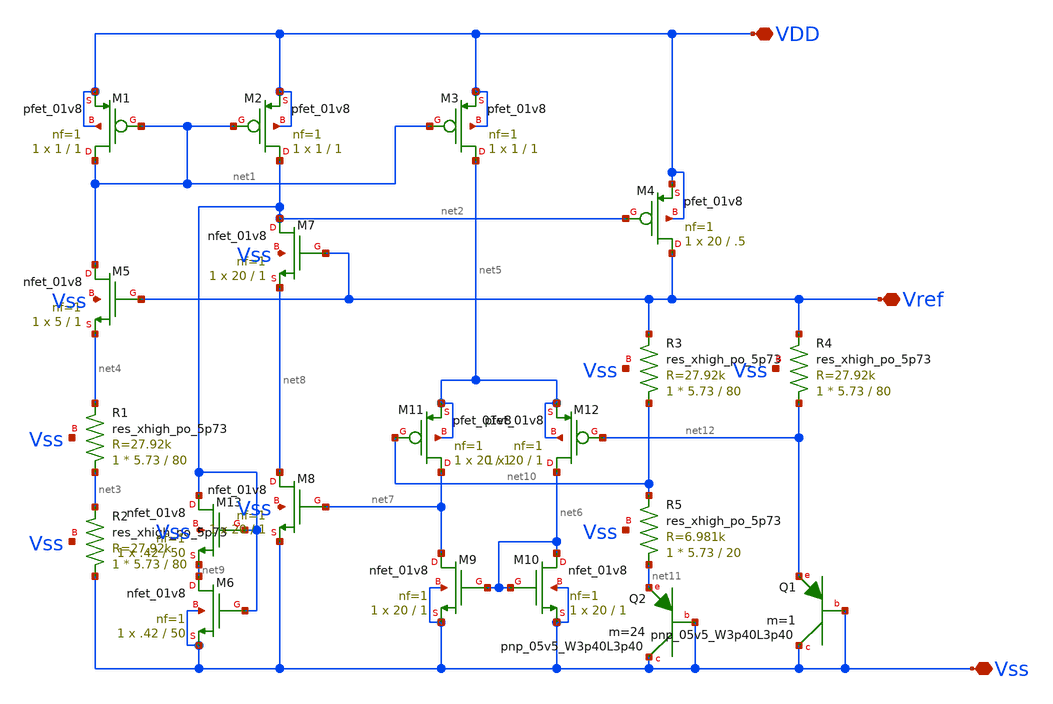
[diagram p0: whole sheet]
** sch_path: hw05/xschem/bandgap.sch
**.subckt bandgap VDD Vss Vref
*.iopin VDD
*.iopin Vss
*.iopin Vref
XM7 net2 Vref net8 Vss sky130_fd_pr__nfet_01v8 L=1 W=20 nf=1 ad='int((nf+1)/2) * W/nf * 0.29' as='int((nf+2)/2) * W/nf * 0.29'
+ pd='2*int((nf+1)/2) * (W/nf + 0.29)' ps='2*int((nf+2)/2) * (W/nf + 0.29)' nrd='0.29 / W' nrs='0.29 / W'
+ sa=0 sb=0 sd=0 mult=1 m=1
XM1 net1 net1 VDD VDD sky130_fd_pr__pfet_01v8 L=1 W=1 nf=1 ad='int((nf+1)/2) * W/nf * 0.29' as='int((nf+2)/2) * W/nf * 0.29'
+ pd='2*int((nf+1)/2) * (W/nf + 0.29)' ps='2*int((nf+2)/2) * (W/nf + 0.29)' nrd='0.29 / W' nrs='0.29 / W'
+ sa=0 sb=0 sd=0 mult=1 m=1
XM2 net2 net1 VDD VDD sky130_fd_pr__pfet_01v8 L=1 W=1 nf=1 ad='int((nf+1)/2) * W/nf * 0.29' as='int((nf+2)/2) * W/nf * 0.29'
+ pd='2*int((nf+1)/2) * (W/nf + 0.29)' ps='2*int((nf+2)/2) * (W/nf + 0.29)' nrd='0.29 / W' nrs='0.29 / W'
+ sa=0 sb=0 sd=0 mult=1 m=1
XM3 net5 net1 VDD VDD sky130_fd_pr__pfet_01v8 L=1 W=1 nf=1 ad='int((nf+1)/2) * W/nf * 0.29' as='int((nf+2)/2) * W/nf * 0.29'
+ pd='2*int((nf+1)/2) * (W/nf + 0.29)' ps='2*int((nf+2)/2) * (W/nf + 0.29)' nrd='0.29 / W' nrs='0.29 / W'
+ sa=0 sb=0 sd=0 mult=1 m=1
XM4 Vref net2 VDD VDD sky130_fd_pr__pfet_01v8 L=.5 W=20 nf=1 ad='int((nf+1)/2) * W/nf * 0.29' as='int((nf+2)/2) * W/nf * 0.29'
+ pd='2*int((nf+1)/2) * (W/nf + 0.29)' ps='2*int((nf+2)/2) * (W/nf + 0.29)' nrd='0.29 / W' nrs='0.29 / W'
+ sa=0 sb=0 sd=0 mult=1 m=1
XM5 net1 Vref net4 Vss sky130_fd_pr__nfet_01v8 L=1 W=5 nf=1 ad='int((nf+1)/2) * W/nf * 0.29' as='int((nf+2)/2) * W/nf * 0.29'
+ pd='2*int((nf+1)/2) * (W/nf + 0.29)' ps='2*int((nf+2)/2) * (W/nf + 0.29)' nrd='0.29 / W' nrs='0.29 / W'
+ sa=0 sb=0 sd=0 mult=1 m=1
XR1 net3 net4 Vss sky130_fd_pr__res_xhigh_po_5p73 L=80 mult=1 m=1
XR2 Vss net3 Vss sky130_fd_pr__res_xhigh_po_5p73 L=80 mult=1 m=1
XM6 net9 net2 Vss Vss sky130_fd_pr__nfet_01v8 L=50 W=.42 nf=1 ad='int((nf+1)/2) * W/nf * 0.29' as='int((nf+2)/2) * W/nf * 0.29'
+ pd='2*int((nf+1)/2) * (W/nf + 0.29)' ps='2*int((nf+2)/2) * (W/nf + 0.29)' nrd='0.29 / W' nrs='0.29 / W'
+ sa=0 sb=0 sd=0 mult=1 m=1
XM8 net8 net7 Vss Vss sky130_fd_pr__nfet_01v8 L=1 W=20 nf=1 ad='int((nf+1)/2) * W/nf * 0.29' as='int((nf+2)/2) * W/nf * 0.29'
+ pd='2*int((nf+1)/2) * (W/nf + 0.29)' ps='2*int((nf+2)/2) * (W/nf + 0.29)' nrd='0.29 / W' nrs='0.29 / W'
+ sa=0 sb=0 sd=0 mult=1 m=1
XM9 net7 net6 Vss Vss sky130_fd_pr__nfet_01v8 L=1 W=20 nf=1 ad='int((nf+1)/2) * W/nf * 0.29' as='int((nf+2)/2) * W/nf * 0.29'
+ pd='2*int((nf+1)/2) * (W/nf + 0.29)' ps='2*int((nf+2)/2) * (W/nf + 0.29)' nrd='0.29 / W' nrs='0.29 / W'
+ sa=0 sb=0 sd=0 mult=1 m=1
XM10 net6 net6 Vss Vss sky130_fd_pr__nfet_01v8 L=1 W=20 nf=1 ad='int((nf+1)/2) * W/nf * 0.29' as='int((nf+2)/2) * W/nf * 0.29'
+ pd='2*int((nf+1)/2) * (W/nf + 0.29)' ps='2*int((nf+2)/2) * (W/nf + 0.29)' nrd='0.29 / W' nrs='0.29 / W'
+ sa=0 sb=0 sd=0 mult=1 m=1
XM11 net7 net10 net5 net5 sky130_fd_pr__pfet_01v8 L=1 W=20 nf=1 ad='int((nf+1)/2) * W/nf * 0.29' as='int((nf+2)/2) * W/nf * 0.29'
+ pd='2*int((nf+1)/2) * (W/nf + 0.29)' ps='2*int((nf+2)/2) * (W/nf + 0.29)' nrd='0.29 / W' nrs='0.29 / W'
+ sa=0 sb=0 sd=0 mult=1 m=1
XM12 net6 net12 net5 net5 sky130_fd_pr__pfet_01v8 L=1 W=20 nf=1 ad='int((nf+1)/2) * W/nf * 0.29' as='int((nf+2)/2) * W/nf * 0.29'
+ pd='2*int((nf+1)/2) * (W/nf + 0.29)' ps='2*int((nf+2)/2) * (W/nf + 0.29)' nrd='0.29 / W' nrs='0.29 / W'
+ sa=0 sb=0 sd=0 mult=1 m=1
XM13 net2 net2 net9 Vss sky130_fd_pr__nfet_01v8 L=50 W=.42 nf=1 ad='int((nf+1)/2) * W/nf * 0.29' as='int((nf+2)/2) * W/nf * 0.29'
+ pd='2*int((nf+1)/2) * (W/nf + 0.29)' ps='2*int((nf+2)/2) * (W/nf + 0.29)' nrd='0.29 / W' nrs='0.29 / W'
+ sa=0 sb=0 sd=0 mult=1 m=1
XR3 net10 Vref Vss sky130_fd_pr__res_xhigh_po_5p73 L=80 mult=1 m=1
XR4 net12 Vref Vss sky130_fd_pr__res_xhigh_po_5p73 L=80 mult=1 m=1
XR5 net11 net10 Vss sky130_fd_pr__res_xhigh_po_5p73 L=20 mult=1 m=1
XQ1 Vss Vss net12 sky130_fd_pr__pnp_05v5_W3p40L3p40 m=1
XQ2 Vss Vss net11 sky130_fd_pr__pnp_05v5_W3p40L3p40 m=24
**.ends
.end
